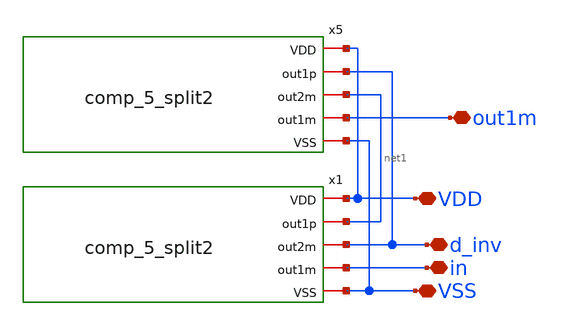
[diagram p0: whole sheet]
** sch_path: 5_Design/4_Layout/Team 5/splitUpSimulationsAndSchematics/comp_5_splitTop2.sch
**.subckt comp_5_splitTop2 VDD d_inv VSS out1m in
*.iopin VDD
*.iopin d_inv
*.iopin VSS
*.iopin out1m
*.iopin in
x1 VDD net1 d_inv in VSS comp_5_split2
x5 VDD d_inv net1 out1m VSS comp_5_split2
**.ends
.end
